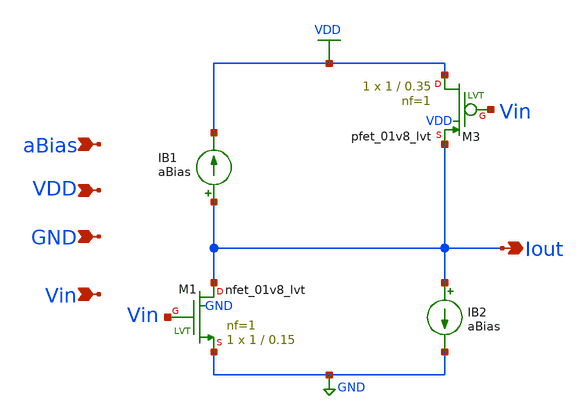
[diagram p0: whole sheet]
** sch_path: VI_Converter.sch
**.subckt VI_Converter Iout Vin VDD GND aBias
*.opin Iout
*.ipin Vin
*.ipin VDD
*.ipin GND
*.ipin aBias
IB1 Iout VDD aBias
XM1 Iout Vin GND GND sky130_fd_pr__nfet_01v8_lvt L=0.15 W=1 nf=1 ad='int((1 + 1)/2) * 1 / 1 * 0.29' as='int((1 + 2)/2) * 1 / 1 * 0.29'
+ pd='2*int((1 + 1)/2) * (1 / 1 + 0.29)' ps='2*int((1 + 2)/2) * (1 / 1 + 0.29)' nrd='0.29 / 1 ' nrs='0.29 / 1 '
+ sa=0 sb=0 sd=0 mult=1 m=1
XM3 VDD Vin Iout VDD sky130_fd_pr__pfet_01v8_lvt L=0.35 W=1 nf=1 ad='int((1 + 1)/2) * 1 / 1 * 0.29' as='int((1 + 2)/2) * 1 / 1 * 0.29'
+ pd='2*int((1 + 1)/2) * (1 / 1 + 0.29)' ps='2*int((1 + 2)/2) * (1 / 1 + 0.29)' nrd='0.29 / 1 ' nrs='0.29 / 1 '
+ sa=0 sb=0 sd=0 mult=1 m=1
IB2 Iout GND aBias
**.ends
.GLOBAL VDD
.GLOBAL GND
.end
